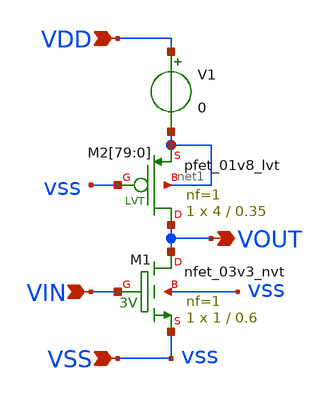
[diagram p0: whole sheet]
** sch_path: design/THESIS_EXP_RO_INVERTER_SKY130A/INV_NVT_diode.sch
**.subckt INV_NVT_diode VDD VSS VIN VOUT
*.ipin VDD
*.ipin VSS
*.ipin VIN
*.opin VOUT
XM1 VOUT VIN VSS vss sky130_fd_pr__nfet_03v3_nvt L=0.6 W=1 nf=1 ad='int((nf+1)/2) * W/nf * 0.29' as='int((nf+2)/2) * W/nf * 0.29'
+ pd='2*int((nf+1)/2) * (W/nf + 0.29)' ps='2*int((nf+2)/2) * (W/nf + 0.29)' nrd='0.29 / W' nrs='0.29 / W'
+ sa=0 sb=0 sd=0 mult=1 m=1
V1 VDD net1 0
.save i(v1)
XM2[79] VOUT vss net1 net1 sky130_fd_pr__pfet_01v8_lvt L=0.35 W=4 nf=1 ad='int((nf+1)/2) * W/nf * 0.29'
+ as='int((nf+2)/2) * W/nf * 0.29' pd='2*int((nf+1)/2) * (W/nf + 0.29)' ps='2*int((nf+2)/2) * (W/nf + 0.29)'
+ nrd='0.29 / W' nrs='0.29 / W' sa=0 sb=0 sd=0 mult=1 m=1
XM2[78] VOUT vss net1 net1 sky130_fd_pr__pfet_01v8_lvt L=0.35 W=4 nf=1 ad='int((nf+1)/2) * W/nf * 0.29'
+ as='int((nf+2)/2) * W/nf * 0.29' pd='2*int((nf+1)/2) * (W/nf + 0.29)' ps='2*int((nf+2)/2) * (W/nf + 0.29)'
+ nrd='0.29 / W' nrs='0.29 / W' sa=0 sb=0 sd=0 mult=1 m=1
XM2[77] VOUT vss net1 net1 sky130_fd_pr__pfet_01v8_lvt L=0.35 W=4 nf=1 ad='int((nf+1)/2) * W/nf * 0.29'
+ as='int((nf+2)/2) * W/nf * 0.29' pd='2*int((nf+1)/2) * (W/nf + 0.29)' ps='2*int((nf+2)/2) * (W/nf + 0.29)'
+ nrd='0.29 / W' nrs='0.29 / W' sa=0 sb=0 sd=0 mult=1 m=1
XM2[76] VOUT vss net1 net1 sky130_fd_pr__pfet_01v8_lvt L=0.35 W=4 nf=1 ad='int((nf+1)/2) * W/nf * 0.29'
+ as='int((nf+2)/2) * W/nf * 0.29' pd='2*int((nf+1)/2) * (W/nf + 0.29)' ps='2*int((nf+2)/2) * (W/nf + 0.29)'
+ nrd='0.29 / W' nrs='0.29 / W' sa=0 sb=0 sd=0 mult=1 m=1
XM2[75] VOUT vss net1 net1 sky130_fd_pr__pfet_01v8_lvt L=0.35 W=4 nf=1 ad='int((nf+1)/2) * W/nf * 0.29'
+ as='int((nf+2)/2) * W/nf * 0.29' pd='2*int((nf+1)/2) * (W/nf + 0.29)' ps='2*int((nf+2)/2) * (W/nf + 0.29)'
+ nrd='0.29 / W' nrs='0.29 / W' sa=0 sb=0 sd=0 mult=1 m=1
XM2[74] VOUT vss net1 net1 sky130_fd_pr__pfet_01v8_lvt L=0.35 W=4 nf=1 ad='int((nf+1)/2) * W/nf * 0.29'
+ as='int((nf+2)/2) * W/nf * 0.29' pd='2*int((nf+1)/2) * (W/nf + 0.29)' ps='2*int((nf+2)/2) * (W/nf + 0.29)'
+ nrd='0.29 / W' nrs='0.29 / W' sa=0 sb=0 sd=0 mult=1 m=1
XM2[73] VOUT vss net1 net1 sky130_fd_pr__pfet_01v8_lvt L=0.35 W=4 nf=1 ad='int((nf+1)/2) * W/nf * 0.29'
+ as='int((nf+2)/2) * W/nf * 0.29' pd='2*int((nf+1)/2) * (W/nf + 0.29)' ps='2*int((nf+2)/2) * (W/nf + 0.29)'
+ nrd='0.29 / W' nrs='0.29 / W' sa=0 sb=0 sd=0 mult=1 m=1
XM2[72] VOUT vss net1 net1 sky130_fd_pr__pfet_01v8_lvt L=0.35 W=4 nf=1 ad='int((nf+1)/2) * W/nf * 0.29'
+ as='int((nf+2)/2) * W/nf * 0.29' pd='2*int((nf+1)/2) * (W/nf + 0.29)' ps='2*int((nf+2)/2) * (W/nf + 0.29)'
+ nrd='0.29 / W' nrs='0.29 / W' sa=0 sb=0 sd=0 mult=1 m=1
XM2[71] VOUT vss net1 net1 sky130_fd_pr__pfet_01v8_lvt L=0.35 W=4 nf=1 ad='int((nf+1)/2) * W/nf * 0.29'
+ as='int((nf+2)/2) * W/nf * 0.29' pd='2*int((nf+1)/2) * (W/nf + 0.29)' ps='2*int((nf+2)/2) * (W/nf + 0.29)'
+ nrd='0.29 / W' nrs='0.29 / W' sa=0 sb=0 sd=0 mult=1 m=1
XM2[70] VOUT vss net1 net1 sky130_fd_pr__pfet_01v8_lvt L=0.35 W=4 nf=1 ad='int((nf+1)/2) * W/nf * 0.29'
+ as='int((nf+2)/2) * W/nf * 0.29' pd='2*int((nf+1)/2) * (W/nf + 0.29)' ps='2*int((nf+2)/2) * (W/nf + 0.29)'
+ nrd='0.29 / W' nrs='0.29 / W' sa=0 sb=0 sd=0 mult=1 m=1
XM2[69] VOUT vss net1 net1 sky130_fd_pr__pfet_01v8_lvt L=0.35 W=4 nf=1 ad='int((nf+1)/2) * W/nf * 0.29'
+ as='int((nf+2)/2) * W/nf * 0.29' pd='2*int((nf+1)/2) * (W/nf + 0.29)' ps='2*int((nf+2)/2) * (W/nf + 0.29)'
+ nrd='0.29 / W' nrs='0.29 / W' sa=0 sb=0 sd=0 mult=1 m=1
XM2[68] VOUT vss net1 net1 sky130_fd_pr__pfet_01v8_lvt L=0.35 W=4 nf=1 ad='int((nf+1)/2) * W/nf * 0.29'
+ as='int((nf+2)/2) * W/nf * 0.29' pd='2*int((nf+1)/2) * (W/nf + 0.29)' ps='2*int((nf+2)/2) * (W/nf + 0.29)'
+ nrd='0.29 / W' nrs='0.29 / W' sa=0 sb=0 sd=0 mult=1 m=1
XM2[67] VOUT vss net1 net1 sky130_fd_pr__pfet_01v8_lvt L=0.35 W=4 nf=1 ad='int((nf+1)/2) * W/nf * 0.29'
+ as='int((nf+2)/2) * W/nf * 0.29' pd='2*int((nf+1)/2) * (W/nf + 0.29)' ps='2*int((nf+2)/2) * (W/nf + 0.29)'
+ nrd='0.29 / W' nrs='0.29 / W' sa=0 sb=0 sd=0 mult=1 m=1
XM2[66] VOUT vss net1 net1 sky130_fd_pr__pfet_01v8_lvt L=0.35 W=4 nf=1 ad='int((nf+1)/2) * W/nf * 0.29'
+ as='int((nf+2)/2) * W/nf * 0.29' pd='2*int((nf+1)/2) * (W/nf + 0.29)' ps='2*int((nf+2)/2) * (W/nf + 0.29)'
+ nrd='0.29 / W' nrs='0.29 / W' sa=0 sb=0 sd=0 mult=1 m=1
XM2[65] VOUT vss net1 net1 sky130_fd_pr__pfet_01v8_lvt L=0.35 W=4 nf=1 ad='int((nf+1)/2) * W/nf * 0.29'
+ as='int((nf+2)/2) * W/nf * 0.29' pd='2*int((nf+1)/2) * (W/nf + 0.29)' ps='2*int((nf+2)/2) * (W/nf + 0.29)'
+ nrd='0.29 / W' nrs='0.29 / W' sa=0 sb=0 sd=0 mult=1 m=1
XM2[64] VOUT vss net1 net1 sky130_fd_pr__pfet_01v8_lvt L=0.35 W=4 nf=1 ad='int((nf+1)/2) * W/nf * 0.29'
+ as='int((nf+2)/2) * W/nf * 0.29' pd='2*int((nf+1)/2) * (W/nf + 0.29)' ps='2*int((nf+2)/2) * (W/nf + 0.29)'
+ nrd='0.29 / W' nrs='0.29 / W' sa=0 sb=0 sd=0 mult=1 m=1
XM2[63] VOUT vss net1 net1 sky130_fd_pr__pfet_01v8_lvt L=0.35 W=4 nf=1 ad='int((nf+1)/2) * W/nf * 0.29'
+ as='int((nf+2)/2) * W/nf * 0.29' pd='2*int((nf+1)/2) * (W/nf + 0.29)' ps='2*int((nf+2)/2) * (W/nf + 0.29)'
+ nrd='0.29 / W' nrs='0.29 / W' sa=0 sb=0 sd=0 mult=1 m=1
XM2[62] VOUT vss net1 net1 sky130_fd_pr__pfet_01v8_lvt L=0.35 W=4 nf=1 ad='int((nf+1)/2) * W/nf * 0.29'
+ as='int((nf+2)/2) * W/nf * 0.29' pd='2*int((nf+1)/2) * (W/nf + 0.29)' ps='2*int((nf+2)/2) * (W/nf + 0.29)'
+ nrd='0.29 / W' nrs='0.29 / W' sa=0 sb=0 sd=0 mult=1 m=1
XM2[61] VOUT vss net1 net1 sky130_fd_pr__pfet_01v8_lvt L=0.35 W=4 nf=1 ad='int((nf+1)/2) * W/nf * 0.29'
+ as='int((nf+2)/2) * W/nf * 0.29' pd='2*int((nf+1)/2) * (W/nf + 0.29)' ps='2*int((nf+2)/2) * (W/nf + 0.29)'
+ nrd='0.29 / W' nrs='0.29 / W' sa=0 sb=0 sd=0 mult=1 m=1
XM2[60] VOUT vss net1 net1 sky130_fd_pr__pfet_01v8_lvt L=0.35 W=4 nf=1 ad='int((nf+1)/2) * W/nf * 0.29'
+ as='int((nf+2)/2) * W/nf * 0.29' pd='2*int((nf+1)/2) * (W/nf + 0.29)' ps='2*int((nf+2)/2) * (W/nf + 0.29)'
+ nrd='0.29 / W' nrs='0.29 / W' sa=0 sb=0 sd=0 mult=1 m=1
XM2[59] VOUT vss net1 net1 sky130_fd_pr__pfet_01v8_lvt L=0.35 W=4 nf=1 ad='int((nf+1)/2) * W/nf * 0.29'
+ as='int((nf+2)/2) * W/nf * 0.29' pd='2*int((nf+1)/2) * (W/nf + 0.29)' ps='2*int((nf+2)/2) * (W/nf + 0.29)'
+ nrd='0.29 / W' nrs='0.29 / W' sa=0 sb=0 sd=0 mult=1 m=1
XM2[58] VOUT vss net1 net1 sky130_fd_pr__pfet_01v8_lvt L=0.35 W=4 nf=1 ad='int((nf+1)/2) * W/nf * 0.29'
+ as='int((nf+2)/2) * W/nf * 0.29' pd='2*int((nf+1)/2) * (W/nf + 0.29)' ps='2*int((nf+2)/2) * (W/nf + 0.29)'
+ nrd='0.29 / W' nrs='0.29 / W' sa=0 sb=0 sd=0 mult=1 m=1
XM2[57] VOUT vss net1 net1 sky130_fd_pr__pfet_01v8_lvt L=0.35 W=4 nf=1 ad='int((nf+1)/2) * W/nf * 0.29'
+ as='int((nf+2)/2) * W/nf * 0.29' pd='2*int((nf+1)/2) * (W/nf + 0.29)' ps='2*int((nf+2)/2) * (W/nf + 0.29)'
+ nrd='0.29 / W' nrs='0.29 / W' sa=0 sb=0 sd=0 mult=1 m=1
XM2[56] VOUT vss net1 net1 sky130_fd_pr__pfet_01v8_lvt L=0.35 W=4 nf=1 ad='int((nf+1)/2) * W/nf * 0.29'
+ as='int((nf+2)/2) * W/nf * 0.29' pd='2*int((nf+1)/2) * (W/nf + 0.29)' ps='2*int((nf+2)/2) * (W/nf + 0.29)'
+ nrd='0.29 / W' nrs='0.29 / W' sa=0 sb=0 sd=0 mult=1 m=1
XM2[55] VOUT vss net1 net1 sky130_fd_pr__pfet_01v8_lvt L=0.35 W=4 nf=1 ad='int((nf+1)/2) * W/nf * 0.29'
+ as='int((nf+2)/2) * W/nf * 0.29' pd='2*int((nf+1)/2) * (W/nf + 0.29)' ps='2*int((nf+2)/2) * (W/nf + 0.29)'
+ nrd='0.29 / W' nrs='0.29 / W' sa=0 sb=0 sd=0 mult=1 m=1
XM2[54] VOUT vss net1 net1 sky130_fd_pr__pfet_01v8_lvt L=0.35 W=4 nf=1 ad='int((nf+1)/2) * W/nf * 0.29'
+ as='int((nf+2)/2) * W/nf * 0.29' pd='2*int((nf+1)/2) * (W/nf + 0.29)' ps='2*int((nf+2)/2) * (W/nf + 0.29)'
+ nrd='0.29 / W' nrs='0.29 / W' sa=0 sb=0 sd=0 mult=1 m=1
XM2[53] VOUT vss net1 net1 sky130_fd_pr__pfet_01v8_lvt L=0.35 W=4 nf=1 ad='int((nf+1)/2) * W/nf * 0.29'
+ as='int((nf+2)/2) * W/nf * 0.29' pd='2*int((nf+1)/2) * (W/nf + 0.29)' ps='2*int((nf+2)/2) * (W/nf + 0.29)'
+ nrd='0.29 / W' nrs='0.29 / W' sa=0 sb=0 sd=0 mult=1 m=1
XM2[52] VOUT vss net1 net1 sky130_fd_pr__pfet_01v8_lvt L=0.35 W=4 nf=1 ad='int((nf+1)/2) * W/nf * 0.29'
+ as='int((nf+2)/2) * W/nf * 0.29' pd='2*int((nf+1)/2) * (W/nf + 0.29)' ps='2*int((nf+2)/2) * (W/nf + 0.29)'
+ nrd='0.29 / W' nrs='0.29 / W' sa=0 sb=0 sd=0 mult=1 m=1
XM2[51] VOUT vss net1 net1 sky130_fd_pr__pfet_01v8_lvt L=0.35 W=4 nf=1 ad='int((nf+1)/2) * W/nf * 0.29'
+ as='int((nf+2)/2) * W/nf * 0.29' pd='2*int((nf+1)/2) * (W/nf + 0.29)' ps='2*int((nf+2)/2) * (W/nf + 0.29)'
+ nrd='0.29 / W' nrs='0.29 / W' sa=0 sb=0 sd=0 mult=1 m=1
XM2[50] VOUT vss net1 net1 sky130_fd_pr__pfet_01v8_lvt L=0.35 W=4 nf=1 ad='int((nf+1)/2) * W/nf * 0.29'
+ as='int((nf+2)/2) * W/nf * 0.29' pd='2*int((nf+1)/2) * (W/nf + 0.29)' ps='2*int((nf+2)/2) * (W/nf + 0.29)'
+ nrd='0.29 / W' nrs='0.29 / W' sa=0 sb=0 sd=0 mult=1 m=1
XM2[49] VOUT vss net1 net1 sky130_fd_pr__pfet_01v8_lvt L=0.35 W=4 nf=1 ad='int((nf+1)/2) * W/nf * 0.29'
+ as='int((nf+2)/2) * W/nf * 0.29' pd='2*int((nf+1)/2) * (W/nf + 0.29)' ps='2*int((nf+2)/2) * (W/nf + 0.29)'
+ nrd='0.29 / W' nrs='0.29 / W' sa=0 sb=0 sd=0 mult=1 m=1
XM2[48] VOUT vss net1 net1 sky130_fd_pr__pfet_01v8_lvt L=0.35 W=4 nf=1 ad='int((nf+1)/2) * W/nf * 0.29'
+ as='int((nf+2)/2) * W/nf * 0.29' pd='2*int((nf+1)/2) * (W/nf + 0.29)' ps='2*int((nf+2)/2) * (W/nf + 0.29)'
+ nrd='0.29 / W' nrs='0.29 / W' sa=0 sb=0 sd=0 mult=1 m=1
XM2[47] VOUT vss net1 net1 sky130_fd_pr__pfet_01v8_lvt L=0.35 W=4 nf=1 ad='int((nf+1)/2) * W/nf * 0.29'
+ as='int((nf+2)/2) * W/nf * 0.29' pd='2*int((nf+1)/2) * (W/nf + 0.29)' ps='2*int((nf+2)/2) * (W/nf + 0.29)'
+ nrd='0.29 / W' nrs='0.29 / W' sa=0 sb=0 sd=0 mult=1 m=1
XM2[46] VOUT vss net1 net1 sky130_fd_pr__pfet_01v8_lvt L=0.35 W=4 nf=1 ad='int((nf+1)/2) * W/nf * 0.29'
+ as='int((nf+2)/2) * W/nf * 0.29' pd='2*int((nf+1)/2) * (W/nf + 0.29)' ps='2*int((nf+2)/2) * (W/nf + 0.29)'
+ nrd='0.29 / W' nrs='0.29 / W' sa=0 sb=0 sd=0 mult=1 m=1
XM2[45] VOUT vss net1 net1 sky130_fd_pr__pfet_01v8_lvt L=0.35 W=4 nf=1 ad='int((nf+1)/2) * W/nf * 0.29'
+ as='int((nf+2)/2) * W/nf * 0.29' pd='2*int((nf+1)/2) * (W/nf + 0.29)' ps='2*int((nf+2)/2) * (W/nf + 0.29)'
+ nrd='0.29 / W' nrs='0.29 / W' sa=0 sb=0 sd=0 mult=1 m=1
XM2[44] VOUT vss net1 net1 sky130_fd_pr__pfet_01v8_lvt L=0.35 W=4 nf=1 ad='int((nf+1)/2) * W/nf * 0.29'
+ as='int((nf+2)/2) * W/nf * 0.29' pd='2*int((nf+1)/2) * (W/nf + 0.29)' ps='2*int((nf+2)/2) * (W/nf + 0.29)'
+ nrd='0.29 / W' nrs='0.29 / W' sa=0 sb=0 sd=0 mult=1 m=1
XM2[43] VOUT vss net1 net1 sky130_fd_pr__pfet_01v8_lvt L=0.35 W=4 nf=1 ad='int((nf+1)/2) * W/nf * 0.29'
+ as='int((nf+2)/2) * W/nf * 0.29' pd='2*int((nf+1)/2) * (W/nf + 0.29)' ps='2*int((nf+2)/2) * (W/nf + 0.29)'
+ nrd='0.29 / W' nrs='0.29 / W' sa=0 sb=0 sd=0 mult=1 m=1
XM2[42] VOUT vss net1 net1 sky130_fd_pr__pfet_01v8_lvt L=0.35 W=4 nf=1 ad='int((nf+1)/2) * W/nf * 0.29'
+ as='int((nf+2)/2) * W/nf * 0.29' pd='2*int((nf+1)/2) * (W/nf + 0.29)' ps='2*int((nf+2)/2) * (W/nf + 0.29)'
+ nrd='0.29 / W' nrs='0.29 / W' sa=0 sb=0 sd=0 mult=1 m=1
XM2[41] VOUT vss net1 net1 sky130_fd_pr__pfet_01v8_lvt L=0.35 W=4 nf=1 ad='int((nf+1)/2) * W/nf * 0.29'
+ as='int((nf+2)/2) * W/nf * 0.29' pd='2*int((nf+1)/2) * (W/nf + 0.29)' ps='2*int((nf+2)/2) * (W/nf + 0.29)'
+ nrd='0.29 / W' nrs='0.29 / W' sa=0 sb=0 sd=0 mult=1 m=1
XM2[40] VOUT vss net1 net1 sky130_fd_pr__pfet_01v8_lvt L=0.35 W=4 nf=1 ad='int((nf+1)/2) * W/nf * 0.29'
+ as='int((nf+2)/2) * W/nf * 0.29' pd='2*int((nf+1)/2) * (W/nf + 0.29)' ps='2*int((nf+2)/2) * (W/nf + 0.29)'
+ nrd='0.29 / W' nrs='0.29 / W' sa=0 sb=0 sd=0 mult=1 m=1
XM2[39] VOUT vss net1 net1 sky130_fd_pr__pfet_01v8_lvt L=0.35 W=4 nf=1 ad='int((nf+1)/2) * W/nf * 0.29'
+ as='int((nf+2)/2) * W/nf * 0.29' pd='2*int((nf+1)/2) * (W/nf + 0.29)' ps='2*int((nf+2)/2) * (W/nf + 0.29)'
+ nrd='0.29 / W' nrs='0.29 / W' sa=0 sb=0 sd=0 mult=1 m=1
XM2[38] VOUT vss net1 net1 sky130_fd_pr__pfet_01v8_lvt L=0.35 W=4 nf=1 ad='int((nf+1)/2) * W/nf * 0.29'
+ as='int((nf+2)/2) * W/nf * 0.29' pd='2*int((nf+1)/2) * (W/nf + 0.29)' ps='2*int((nf+2)/2) * (W/nf + 0.29)'
+ nrd='0.29 / W' nrs='0.29 / W' sa=0 sb=0 sd=0 mult=1 m=1
XM2[37] VOUT vss net1 net1 sky130_fd_pr__pfet_01v8_lvt L=0.35 W=4 nf=1 ad='int((nf+1)/2) * W/nf * 0.29'
+ as='int((nf+2)/2) * W/nf * 0.29' pd='2*int((nf+1)/2) * (W/nf + 0.29)' ps='2*int((nf+2)/2) * (W/nf + 0.29)'
+ nrd='0.29 / W' nrs='0.29 / W' sa=0 sb=0 sd=0 mult=1 m=1
XM2[36] VOUT vss net1 net1 sky130_fd_pr__pfet_01v8_lvt L=0.35 W=4 nf=1 ad='int((nf+1)/2) * W/nf * 0.29'
+ as='int((nf+2)/2) * W/nf * 0.29' pd='2*int((nf+1)/2) * (W/nf + 0.29)' ps='2*int((nf+2)/2) * (W/nf + 0.29)'
+ nrd='0.29 / W' nrs='0.29 / W' sa=0 sb=0 sd=0 mult=1 m=1
XM2[35] VOUT vss net1 net1 sky130_fd_pr__pfet_01v8_lvt L=0.35 W=4 nf=1 ad='int((nf+1)/2) * W/nf * 0.29'
+ as='int((nf+2)/2) * W/nf * 0.29' pd='2*int((nf+1)/2) * (W/nf + 0.29)' ps='2*int((nf+2)/2) * (W/nf + 0.29)'
+ nrd='0.29 / W' nrs='0.29 / W' sa=0 sb=0 sd=0 mult=1 m=1
XM2[34] VOUT vss net1 net1 sky130_fd_pr__pfet_01v8_lvt L=0.35 W=4 nf=1 ad='int((nf+1)/2) * W/nf * 0.29'
+ as='int((nf+2)/2) * W/nf * 0.29' pd='2*int((nf+1)/2) * (W/nf + 0.29)' ps='2*int((nf+2)/2) * (W/nf + 0.29)'
+ nrd='0.29 / W' nrs='0.29 / W' sa=0 sb=0 sd=0 mult=1 m=1
XM2[33] VOUT vss net1 net1 sky130_fd_pr__pfet_01v8_lvt L=0.35 W=4 nf=1 ad='int((nf+1)/2) * W/nf * 0.29'
+ as='int((nf+2)/2) * W/nf * 0.29' pd='2*int((nf+1)/2) * (W/nf + 0.29)' ps='2*int((nf+2)/2) * (W/nf + 0.29)'
+ nrd='0.29 / W' nrs='0.29 / W' sa=0 sb=0 sd=0 mult=1 m=1
XM2[32] VOUT vss net1 net1 sky130_fd_pr__pfet_01v8_lvt L=0.35 W=4 nf=1 ad='int((nf+1)/2) * W/nf * 0.29'
+ as='int((nf+2)/2) * W/nf * 0.29' pd='2*int((nf+1)/2) * (W/nf + 0.29)' ps='2*int((nf+2)/2) * (W/nf + 0.29)'
+ nrd='0.29 / W' nrs='0.29 / W' sa=0 sb=0 sd=0 mult=1 m=1
XM2[31] VOUT vss net1 net1 sky130_fd_pr__pfet_01v8_lvt L=0.35 W=4 nf=1 ad='int((nf+1)/2) * W/nf * 0.29'
+ as='int((nf+2)/2) * W/nf * 0.29' pd='2*int((nf+1)/2) * (W/nf + 0.29)' ps='2*int((nf+2)/2) * (W/nf + 0.29)'
+ nrd='0.29 / W' nrs='0.29 / W' sa=0 sb=0 sd=0 mult=1 m=1
XM2[30] VOUT vss net1 net1 sky130_fd_pr__pfet_01v8_lvt L=0.35 W=4 nf=1 ad='int((nf+1)/2) * W/nf * 0.29'
+ as='int((nf+2)/2) * W/nf * 0.29' pd='2*int((nf+1)/2) * (W/nf + 0.29)' ps='2*int((nf+2)/2) * (W/nf + 0.29)'
+ nrd='0.29 / W' nrs='0.29 / W' sa=0 sb=0 sd=0 mult=1 m=1
XM2[29] VOUT vss net1 net1 sky130_fd_pr__pfet_01v8_lvt L=0.35 W=4 nf=1 ad='int((nf+1)/2) * W/nf * 0.29'
+ as='int((nf+2)/2) * W/nf * 0.29' pd='2*int((nf+1)/2) * (W/nf + 0.29)' ps='2*int((nf+2)/2) * (W/nf + 0.29)'
+ nrd='0.29 / W' nrs='0.29 / W' sa=0 sb=0 sd=0 mult=1 m=1
XM2[28] VOUT vss net1 net1 sky130_fd_pr__pfet_01v8_lvt L=0.35 W=4 nf=1 ad='int((nf+1)/2) * W/nf * 0.29'
+ as='int((nf+2)/2) * W/nf * 0.29' pd='2*int((nf+1)/2) * (W/nf + 0.29)' ps='2*int((nf+2)/2) * (W/nf + 0.29)'
+ nrd='0.29 / W' nrs='0.29 / W' sa=0 sb=0 sd=0 mult=1 m=1
XM2[27] VOUT vss net1 net1 sky130_fd_pr__pfet_01v8_lvt L=0.35 W=4 nf=1 ad='int((nf+1)/2) * W/nf * 0.29'
+ as='int((nf+2)/2) * W/nf * 0.29' pd='2*int((nf+1)/2) * (W/nf + 0.29)' ps='2*int((nf+2)/2) * (W/nf + 0.29)'
+ nrd='0.29 / W' nrs='0.29 / W' sa=0 sb=0 sd=0 mult=1 m=1
XM2[26] VOUT vss net1 net1 sky130_fd_pr__pfet_01v8_lvt L=0.35 W=4 nf=1 ad='int((nf+1)/2) * W/nf * 0.29'
+ as='int((nf+2)/2) * W/nf * 0.29' pd='2*int((nf+1)/2) * (W/nf + 0.29)' ps='2*int((nf+2)/2) * (W/nf + 0.29)'
+ nrd='0.29 / W' nrs='0.29 / W' sa=0 sb=0 sd=0 mult=1 m=1
XM2[25] VOUT vss net1 net1 sky130_fd_pr__pfet_01v8_lvt L=0.35 W=4 nf=1 ad='int((nf+1)/2) * W/nf * 0.29'
+ as='int((nf+2)/2) * W/nf * 0.29' pd='2*int((nf+1)/2) * (W/nf + 0.29)' ps='2*int((nf+2)/2) * (W/nf + 0.29)'
+ nrd='0.29 / W' nrs='0.29 / W' sa=0 sb=0 sd=0 mult=1 m=1
XM2[24] VOUT vss net1 net1 sky130_fd_pr__pfet_01v8_lvt L=0.35 W=4 nf=1 ad='int((nf+1)/2) * W/nf * 0.29'
+ as='int((nf+2)/2) * W/nf * 0.29' pd='2*int((nf+1)/2) * (W/nf + 0.29)' ps='2*int((nf+2)/2) * (W/nf + 0.29)'
+ nrd='0.29 / W' nrs='0.29 / W' sa=0 sb=0 sd=0 mult=1 m=1
XM2[23] VOUT vss net1 net1 sky130_fd_pr__pfet_01v8_lvt L=0.35 W=4 nf=1 ad='int((nf+1)/2) * W/nf * 0.29'
+ as='int((nf+2)/2) * W/nf * 0.29' pd='2*int((nf+1)/2) * (W/nf + 0.29)' ps='2*int((nf+2)/2) * (W/nf + 0.29)'
+ nrd='0.29 / W' nrs='0.29 / W' sa=0 sb=0 sd=0 mult=1 m=1
XM2[22] VOUT vss net1 net1 sky130_fd_pr__pfet_01v8_lvt L=0.35 W=4 nf=1 ad='int((nf+1)/2) * W/nf * 0.29'
+ as='int((nf+2)/2) * W/nf * 0.29' pd='2*int((nf+1)/2) * (W/nf + 0.29)' ps='2*int((nf+2)/2) * (W/nf + 0.29)'
+ nrd='0.29 / W' nrs='0.29 / W' sa=0 sb=0 sd=0 mult=1 m=1
XM2[21] VOUT vss net1 net1 sky130_fd_pr__pfet_01v8_lvt L=0.35 W=4 nf=1 ad='int((nf+1)/2) * W/nf * 0.29'
+ as='int((nf+2)/2) * W/nf * 0.29' pd='2*int((nf+1)/2) * (W/nf + 0.29)' ps='2*int((nf+2)/2) * (W/nf + 0.29)'
+ nrd='0.29 / W' nrs='0.29 / W' sa=0 sb=0 sd=0 mult=1 m=1
XM2[20] VOUT vss net1 net1 sky130_fd_pr__pfet_01v8_lvt L=0.35 W=4 nf=1 ad='int((nf+1)/2) * W/nf * 0.29'
+ as='int((nf+2)/2) * W/nf * 0.29' pd='2*int((nf+1)/2) * (W/nf + 0.29)' ps='2*int((nf+2)/2) * (W/nf + 0.29)'
+ nrd='0.29 / W' nrs='0.29 / W' sa=0 sb=0 sd=0 mult=1 m=1
XM2[19] VOUT vss net1 net1 sky130_fd_pr__pfet_01v8_lvt L=0.35 W=4 nf=1 ad='int((nf+1)/2) * W/nf * 0.29'
+ as='int((nf+2)/2) * W/nf * 0.29' pd='2*int((nf+1)/2) * (W/nf + 0.29)' ps='2*int((nf+2)/2) * (W/nf + 0.29)'
+ nrd='0.29 / W' nrs='0.29 / W' sa=0 sb=0 sd=0 mult=1 m=1
XM2[18] VOUT vss net1 net1 sky130_fd_pr__pfet_01v8_lvt L=0.35 W=4 nf=1 ad='int((nf+1)/2) * W/nf * 0.29'
+ as='int((nf+2)/2) * W/nf * 0.29' pd='2*int((nf+1)/2) * (W/nf + 0.29)' ps='2*int((nf+2)/2) * (W/nf + 0.29)'
+ nrd='0.29 / W' nrs='0.29 / W' sa=0 sb=0 sd=0 mult=1 m=1
XM2[17] VOUT vss net1 net1 sky130_fd_pr__pfet_01v8_lvt L=0.35 W=4 nf=1 ad='int((nf+1)/2) * W/nf * 0.29'
+ as='int((nf+2)/2) * W/nf * 0.29' pd='2*int((nf+1)/2) * (W/nf + 0.29)' ps='2*int((nf+2)/2) * (W/nf + 0.29)'
+ nrd='0.29 / W' nrs='0.29 / W' sa=0 sb=0 sd=0 mult=1 m=1
XM2[16] VOUT vss net1 net1 sky130_fd_pr__pfet_01v8_lvt L=0.35 W=4 nf=1 ad='int((nf+1)/2) * W/nf * 0.29'
+ as='int((nf+2)/2) * W/nf * 0.29' pd='2*int((nf+1)/2) * (W/nf + 0.29)' ps='2*int((nf+2)/2) * (W/nf + 0.29)'
+ nrd='0.29 / W' nrs='0.29 / W' sa=0 sb=0 sd=0 mult=1 m=1
XM2[15] VOUT vss net1 net1 sky130_fd_pr__pfet_01v8_lvt L=0.35 W=4 nf=1 ad='int((nf+1)/2) * W/nf * 0.29'
+ as='int((nf+2)/2) * W/nf * 0.29' pd='2*int((nf+1)/2) * (W/nf + 0.29)' ps='2*int((nf+2)/2) * (W/nf + 0.29)'
+ nrd='0.29 / W' nrs='0.29 / W' sa=0 sb=0 sd=0 mult=1 m=1
XM2[14] VOUT vss net1 net1 sky130_fd_pr__pfet_01v8_lvt L=0.35 W=4 nf=1 ad='int((nf+1)/2) * W/nf * 0.29'
+ as='int((nf+2)/2) * W/nf * 0.29' pd='2*int((nf+1)/2) * (W/nf + 0.29)' ps='2*int((nf+2)/2) * (W/nf + 0.29)'
+ nrd='0.29 / W' nrs='0.29 / W' sa=0 sb=0 sd=0 mult=1 m=1
XM2[13] VOUT vss net1 net1 sky130_fd_pr__pfet_01v8_lvt L=0.35 W=4 nf=1 ad='int((nf+1)/2) * W/nf * 0.29'
+ as='int((nf+2)/2) * W/nf * 0.29' pd='2*int((nf+1)/2) * (W/nf + 0.29)' ps='2*int((nf+2)/2) * (W/nf + 0.29)'
+ nrd='0.29 / W' nrs='0.29 / W' sa=0 sb=0 sd=0 mult=1 m=1
XM2[12] VOUT vss net1 net1 sky130_fd_pr__pfet_01v8_lvt L=0.35 W=4 nf=1 ad='int((nf+1)/2) * W/nf * 0.29'
+ as='int((nf+2)/2) * W/nf * 0.29' pd='2*int((nf+1)/2) * (W/nf + 0.29)' ps='2*int((nf+2)/2) * (W/nf + 0.29)'
+ nrd='0.29 / W' nrs='0.29 / W' sa=0 sb=0 sd=0 mult=1 m=1
XM2[11] VOUT vss net1 net1 sky130_fd_pr__pfet_01v8_lvt L=0.35 W=4 nf=1 ad='int((nf+1)/2) * W/nf * 0.29'
+ as='int((nf+2)/2) * W/nf * 0.29' pd='2*int((nf+1)/2) * (W/nf + 0.29)' ps='2*int((nf+2)/2) * (W/nf + 0.29)'
+ nrd='0.29 / W' nrs='0.29 / W' sa=0 sb=0 sd=0 mult=1 m=1
XM2[10] VOUT vss net1 net1 sky130_fd_pr__pfet_01v8_lvt L=0.35 W=4 nf=1 ad='int((nf+1)/2) * W/nf * 0.29'
+ as='int((nf+2)/2) * W/nf * 0.29' pd='2*int((nf+1)/2) * (W/nf + 0.29)' ps='2*int((nf+2)/2) * (W/nf + 0.29)'
+ nrd='0.29 / W' nrs='0.29 / W' sa=0 sb=0 sd=0 mult=1 m=1
XM2[9] VOUT vss net1 net1 sky130_fd_pr__pfet_01v8_lvt L=0.35 W=4 nf=1 ad='int((nf+1)/2) * W/nf * 0.29'
+ as='int((nf+2)/2) * W/nf * 0.29' pd='2*int((nf+1)/2) * (W/nf + 0.29)' ps='2*int((nf+2)/2) * (W/nf + 0.29)'
+ nrd='0.29 / W' nrs='0.29 / W' sa=0 sb=0 sd=0 mult=1 m=1
XM2[8] VOUT vss net1 net1 sky130_fd_pr__pfet_01v8_lvt L=0.35 W=4 nf=1 ad='int((nf+1)/2) * W/nf * 0.29'
+ as='int((nf+2)/2) * W/nf * 0.29' pd='2*int((nf+1)/2) * (W/nf + 0.29)' ps='2*int((nf+2)/2) * (W/nf + 0.29)'
+ nrd='0.29 / W' nrs='0.29 / W' sa=0 sb=0 sd=0 mult=1 m=1
XM2[7] VOUT vss net1 net1 sky130_fd_pr__pfet_01v8_lvt L=0.35 W=4 nf=1 ad='int((nf+1)/2) * W/nf * 0.29'
+ as='int((nf+2)/2) * W/nf * 0.29' pd='2*int((nf+1)/2) * (W/nf + 0.29)' ps='2*int((nf+2)/2) * (W/nf + 0.29)'
+ nrd='0.29 / W' nrs='0.29 / W' sa=0 sb=0 sd=0 mult=1 m=1
XM2[6] VOUT vss net1 net1 sky130_fd_pr__pfet_01v8_lvt L=0.35 W=4 nf=1 ad='int((nf+1)/2) * W/nf * 0.29'
+ as='int((nf+2)/2) * W/nf * 0.29' pd='2*int((nf+1)/2) * (W/nf + 0.29)' ps='2*int((nf+2)/2) * (W/nf + 0.29)'
+ nrd='0.29 / W' nrs='0.29 / W' sa=0 sb=0 sd=0 mult=1 m=1
XM2[5] VOUT vss net1 net1 sky130_fd_pr__pfet_01v8_lvt L=0.35 W=4 nf=1 ad='int((nf+1)/2) * W/nf * 0.29'
+ as='int((nf+2)/2) * W/nf * 0.29' pd='2*int((nf+1)/2) * (W/nf + 0.29)' ps='2*int((nf+2)/2) * (W/nf + 0.29)'
+ nrd='0.29 / W' nrs='0.29 / W' sa=0 sb=0 sd=0 mult=1 m=1
XM2[4] VOUT vss net1 net1 sky130_fd_pr__pfet_01v8_lvt L=0.35 W=4 nf=1 ad='int((nf+1)/2) * W/nf * 0.29'
+ as='int((nf+2)/2) * W/nf * 0.29' pd='2*int((nf+1)/2) * (W/nf + 0.29)' ps='2*int((nf+2)/2) * (W/nf + 0.29)'
+ nrd='0.29 / W' nrs='0.29 / W' sa=0 sb=0 sd=0 mult=1 m=1
XM2[3] VOUT vss net1 net1 sky130_fd_pr__pfet_01v8_lvt L=0.35 W=4 nf=1 ad='int((nf+1)/2) * W/nf * 0.29'
+ as='int((nf+2)/2) * W/nf * 0.29' pd='2*int((nf+1)/2) * (W/nf + 0.29)' ps='2*int((nf+2)/2) * (W/nf + 0.29)'
+ nrd='0.29 / W' nrs='0.29 / W' sa=0 sb=0 sd=0 mult=1 m=1
XM2[2] VOUT vss net1 net1 sky130_fd_pr__pfet_01v8_lvt L=0.35 W=4 nf=1 ad='int((nf+1)/2) * W/nf * 0.29'
+ as='int((nf+2)/2) * W/nf * 0.29' pd='2*int((nf+1)/2) * (W/nf + 0.29)' ps='2*int((nf+2)/2) * (W/nf + 0.29)'
+ nrd='0.29 / W' nrs='0.29 / W' sa=0 sb=0 sd=0 mult=1 m=1
XM2[1] VOUT vss net1 net1 sky130_fd_pr__pfet_01v8_lvt L=0.35 W=4 nf=1 ad='int((nf+1)/2) * W/nf * 0.29'
+ as='int((nf+2)/2) * W/nf * 0.29' pd='2*int((nf+1)/2) * (W/nf + 0.29)' ps='2*int((nf+2)/2) * (W/nf + 0.29)'
+ nrd='0.29 / W' nrs='0.29 / W' sa=0 sb=0 sd=0 mult=1 m=1
XM2[0] VOUT vss net1 net1 sky130_fd_pr__pfet_01v8_lvt L=0.35 W=4 nf=1 ad='int((nf+1)/2) * W/nf * 0.29'
+ as='int((nf+2)/2) * W/nf * 0.29' pd='2*int((nf+1)/2) * (W/nf + 0.29)' ps='2*int((nf+2)/2) * (W/nf + 0.29)'
+ nrd='0.29 / W' nrs='0.29 / W' sa=0 sb=0 sd=0 mult=1 m=1
**.ends
.end
